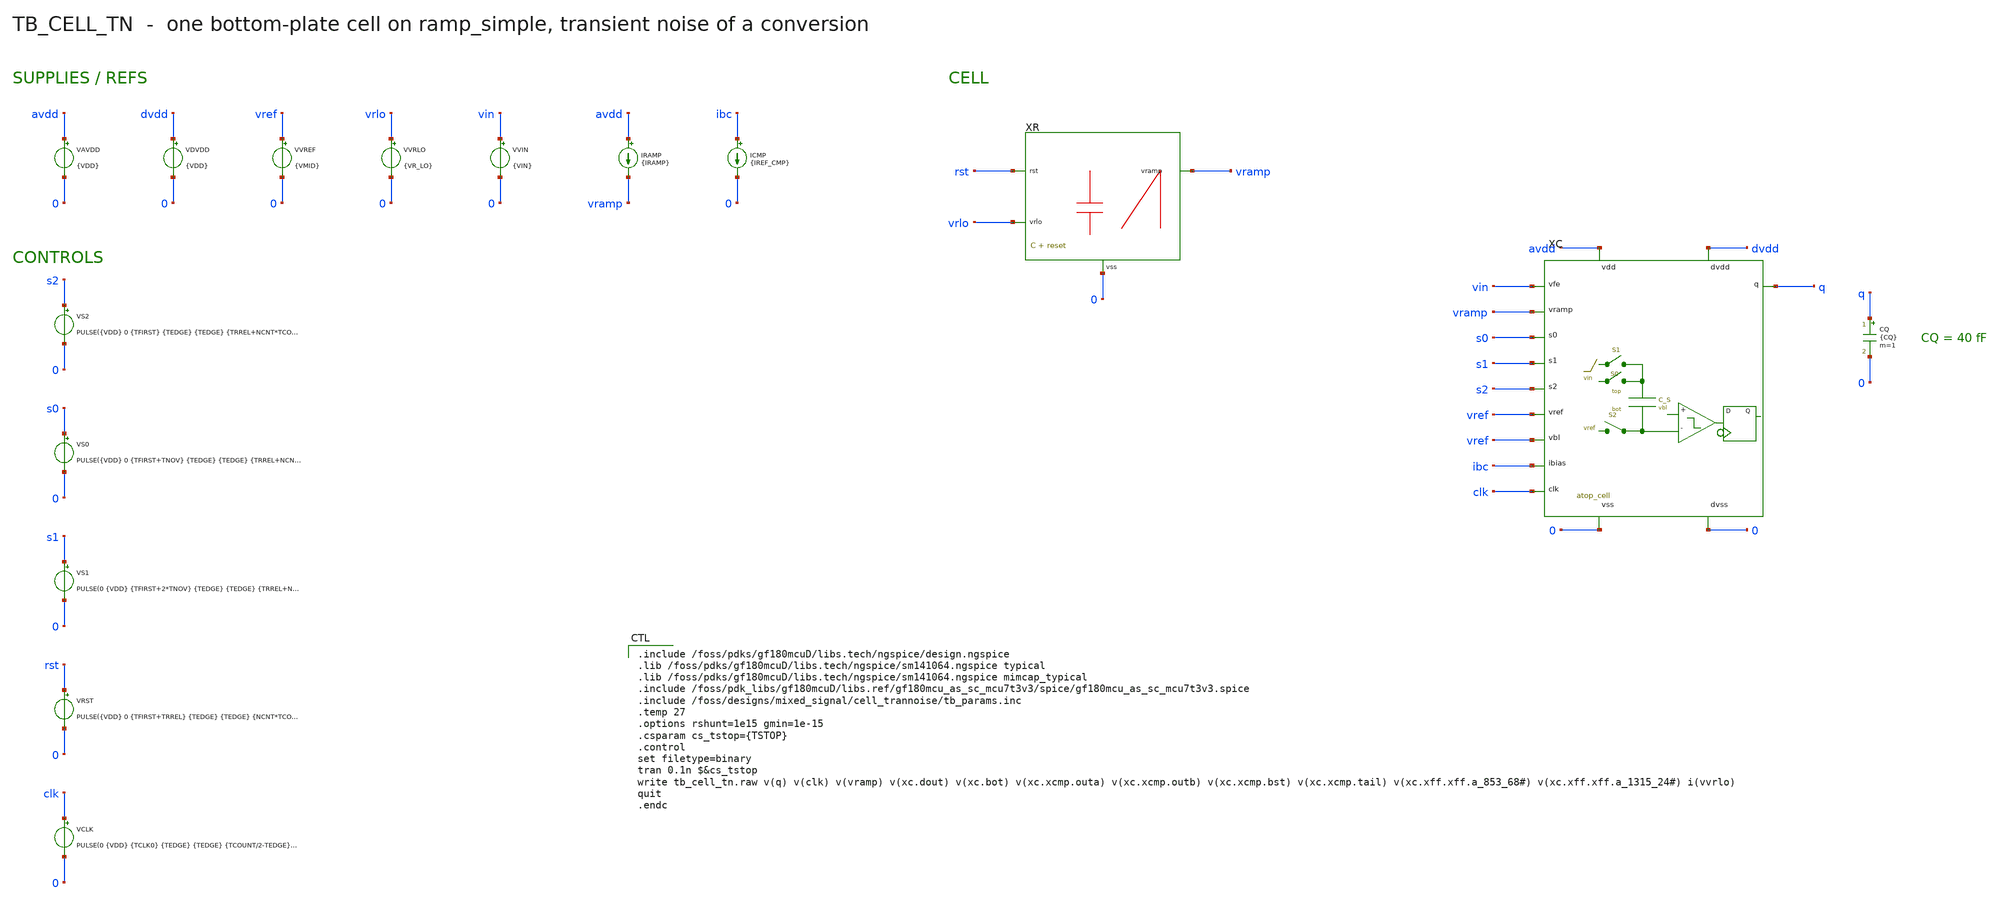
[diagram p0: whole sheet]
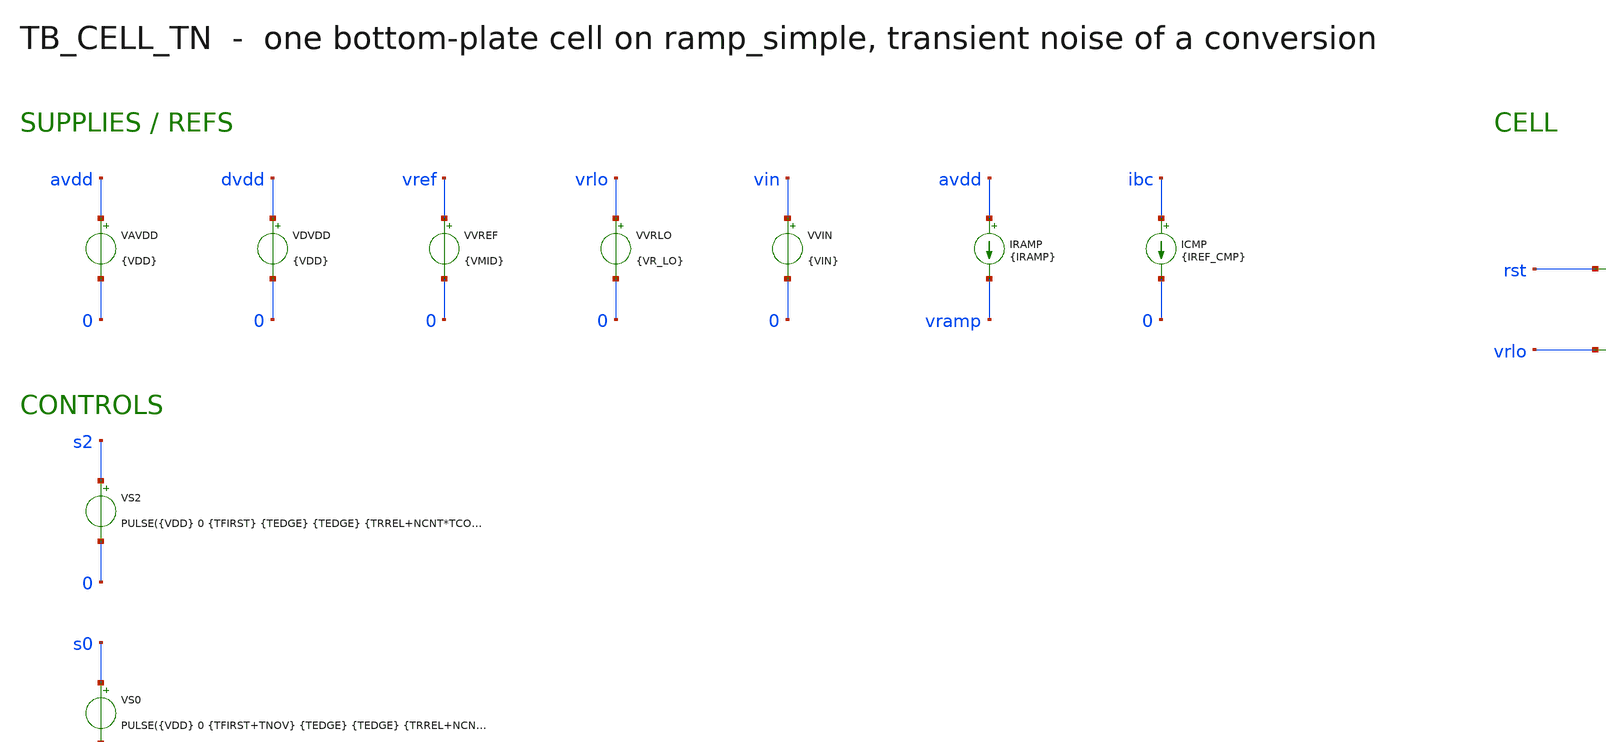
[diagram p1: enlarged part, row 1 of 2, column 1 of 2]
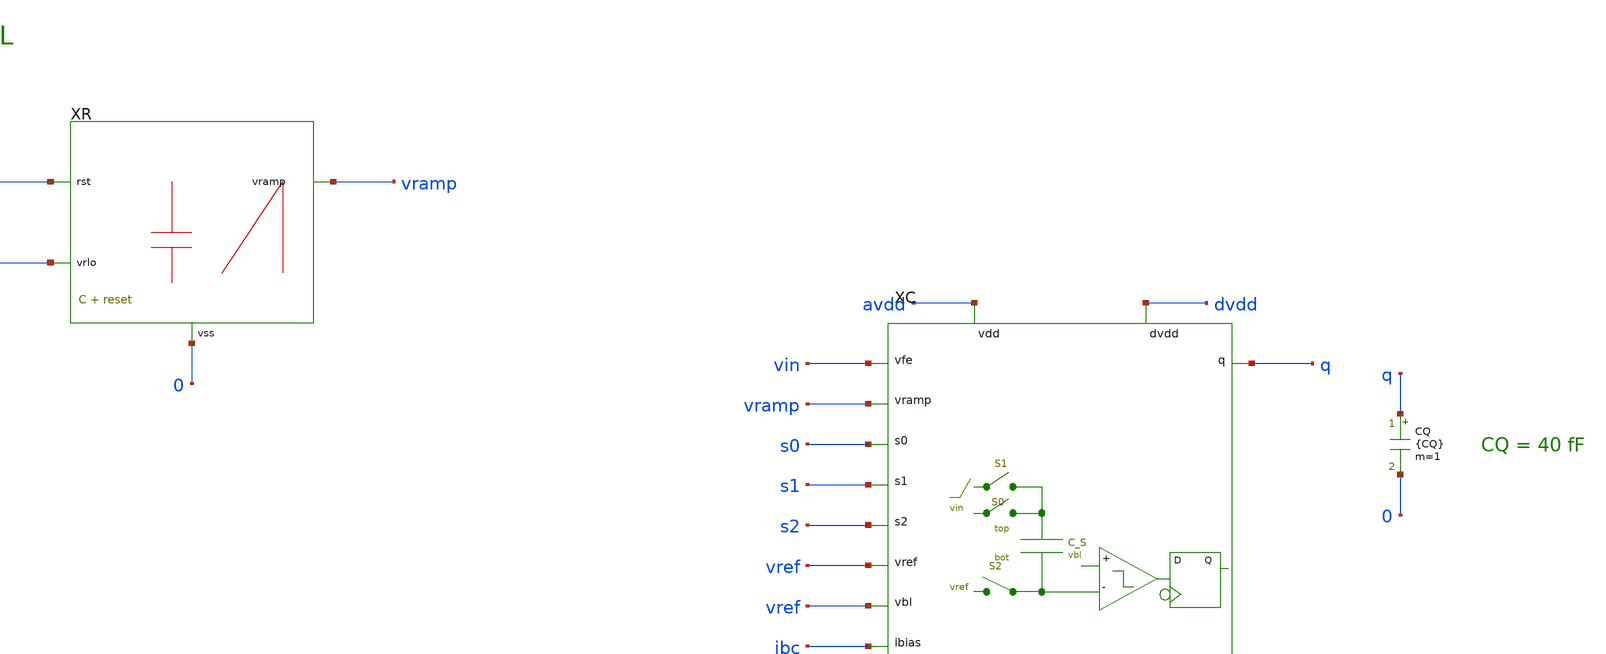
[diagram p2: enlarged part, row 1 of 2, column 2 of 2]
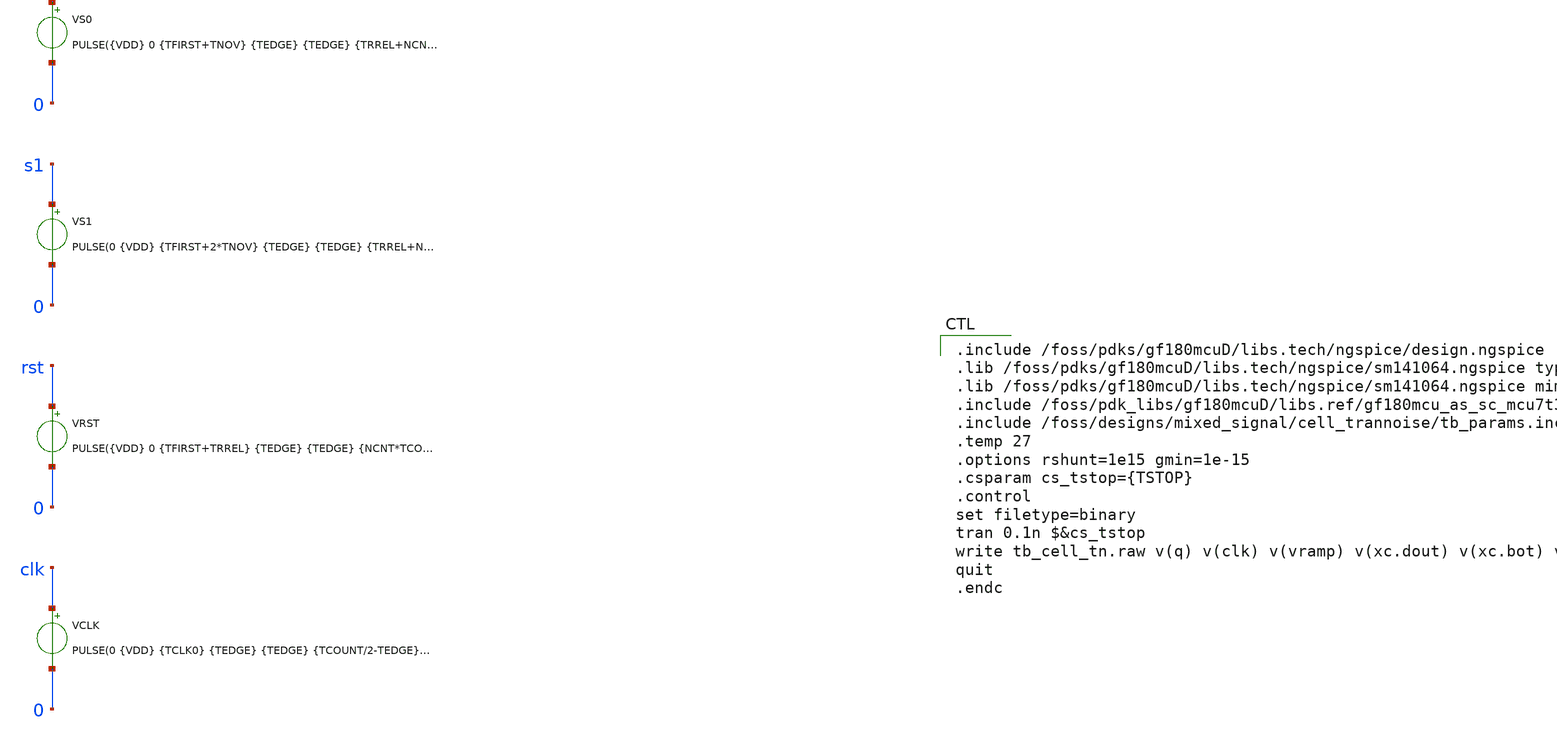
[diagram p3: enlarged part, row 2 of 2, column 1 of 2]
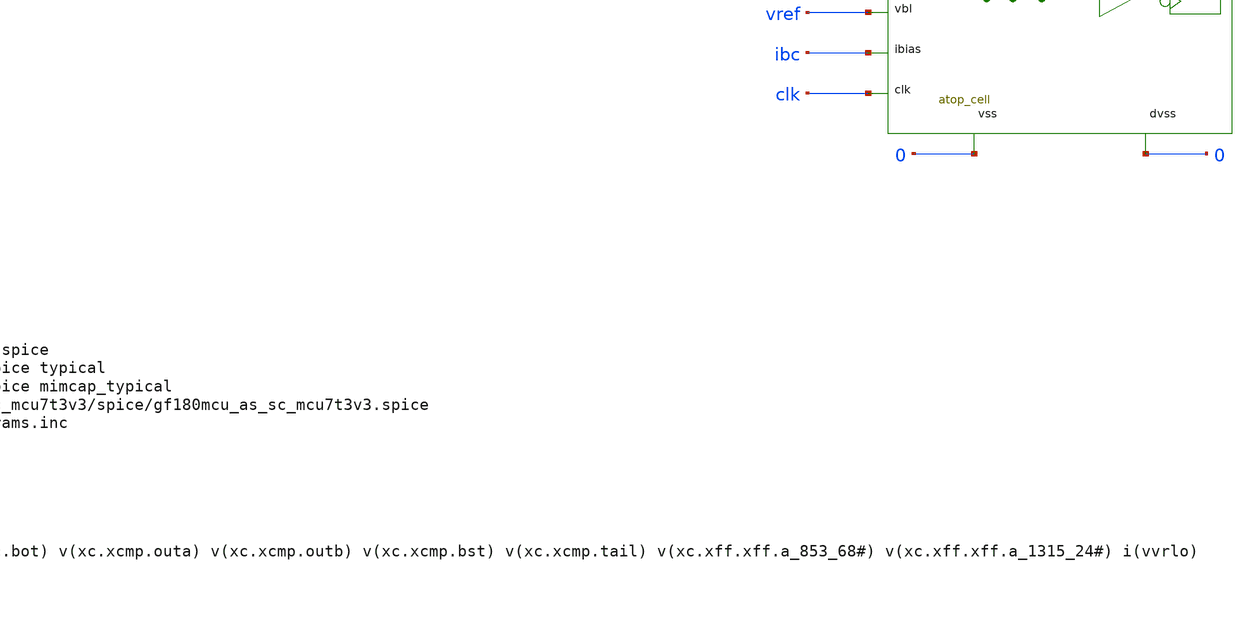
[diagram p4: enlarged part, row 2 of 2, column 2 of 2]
** sch_path: mixed_signal/cell_trannoise/tb_cell_tn.sch
**.subckt tb_cell_tn
VAVDD avdd 0 {VDD}
VDVDD dvdd 0 {VDD}
VVREF vref 0 {VMID}
VVRLO vrlo 0 {VR_LO}
VVIN vin 0 {VIN}
IRAMP avdd vramp {IRAMP}
ICMP ibc 0 {IREF_CMP}
VS2 s2 0 PULSE({VDD} 0 {TFIRST} {TEDGE} {TEDGE} {TRREL+NCNT*TCOUNT+10n-TEDGE} {PCONV})
VS0 s0 0 PULSE({VDD} 0 {TFIRST+TNOV} {TEDGE} {TEDGE} {TRREL+NCNT*TCOUNT+10n-TEDGE-TNOV} {PCONV})
VS1 s1 0 PULSE(0 {VDD} {TFIRST+2*TNOV} {TEDGE} {TEDGE} {TRREL+NCNT*TCOUNT-2*TNOV-TEDGE} {PCONV})
VRST rst 0 PULSE({VDD} 0 {TFIRST+TRREL} {TEDGE} {TEDGE} {NCNT*TCOUNT+5n-TEDGE} {PCONV})
VCLK clk 0 PULSE(0 {VDD} {TCLK0} {TEDGE} {TEDGE} {TCOUNT/2-TEDGE} {TCOUNT})
XR vramp rst vrlo 0 ramp_simple
XC vin vramp s0 s1 s2 vref vref ibc q clk avdd 0 dvdd 0 atop_cell
CQ q 0 {CQ} m=1
**** begin user architecture code

.include /foss/pdks/gf180mcuD/libs.tech/ngspice/design.ngspice
.lib /foss/pdks/gf180mcuD/libs.tech/ngspice/sm141064.ngspice typical
.lib /foss/pdks/gf180mcuD/libs.tech/ngspice/sm141064.ngspice mimcap_typical
.include /foss/pdk_libs/gf180mcuD/libs.ref/gf180mcu_as_sc_mcu7t3v3/spice/gf180mcu_as_sc_mcu7t3v3.spice
.include /foss/designs/mixed_signal/cell_trannoise/tb_params.inc
.temp 27
.options rshunt=1e15 gmin=1e-15
.csparam cs_tstop={TSTOP}
.control
set filetype=binary
tran 0.1n $&cs_tstop
write tb_cell_tn.raw v(q) v(clk) v(vramp) v(xc.dout) v(xc.bot) v(xc.xcmp.outa) v(xc.xcmp.outb)
+ v(xc.xcmp.bst) v(xc.xcmp.tail) v(xc.xff.xff.a_853_68#) v(xc.xff.xff.a_1315_24#) i(vvrlo)
quit
.endc

**** end user architecture code
**.ends
.end
